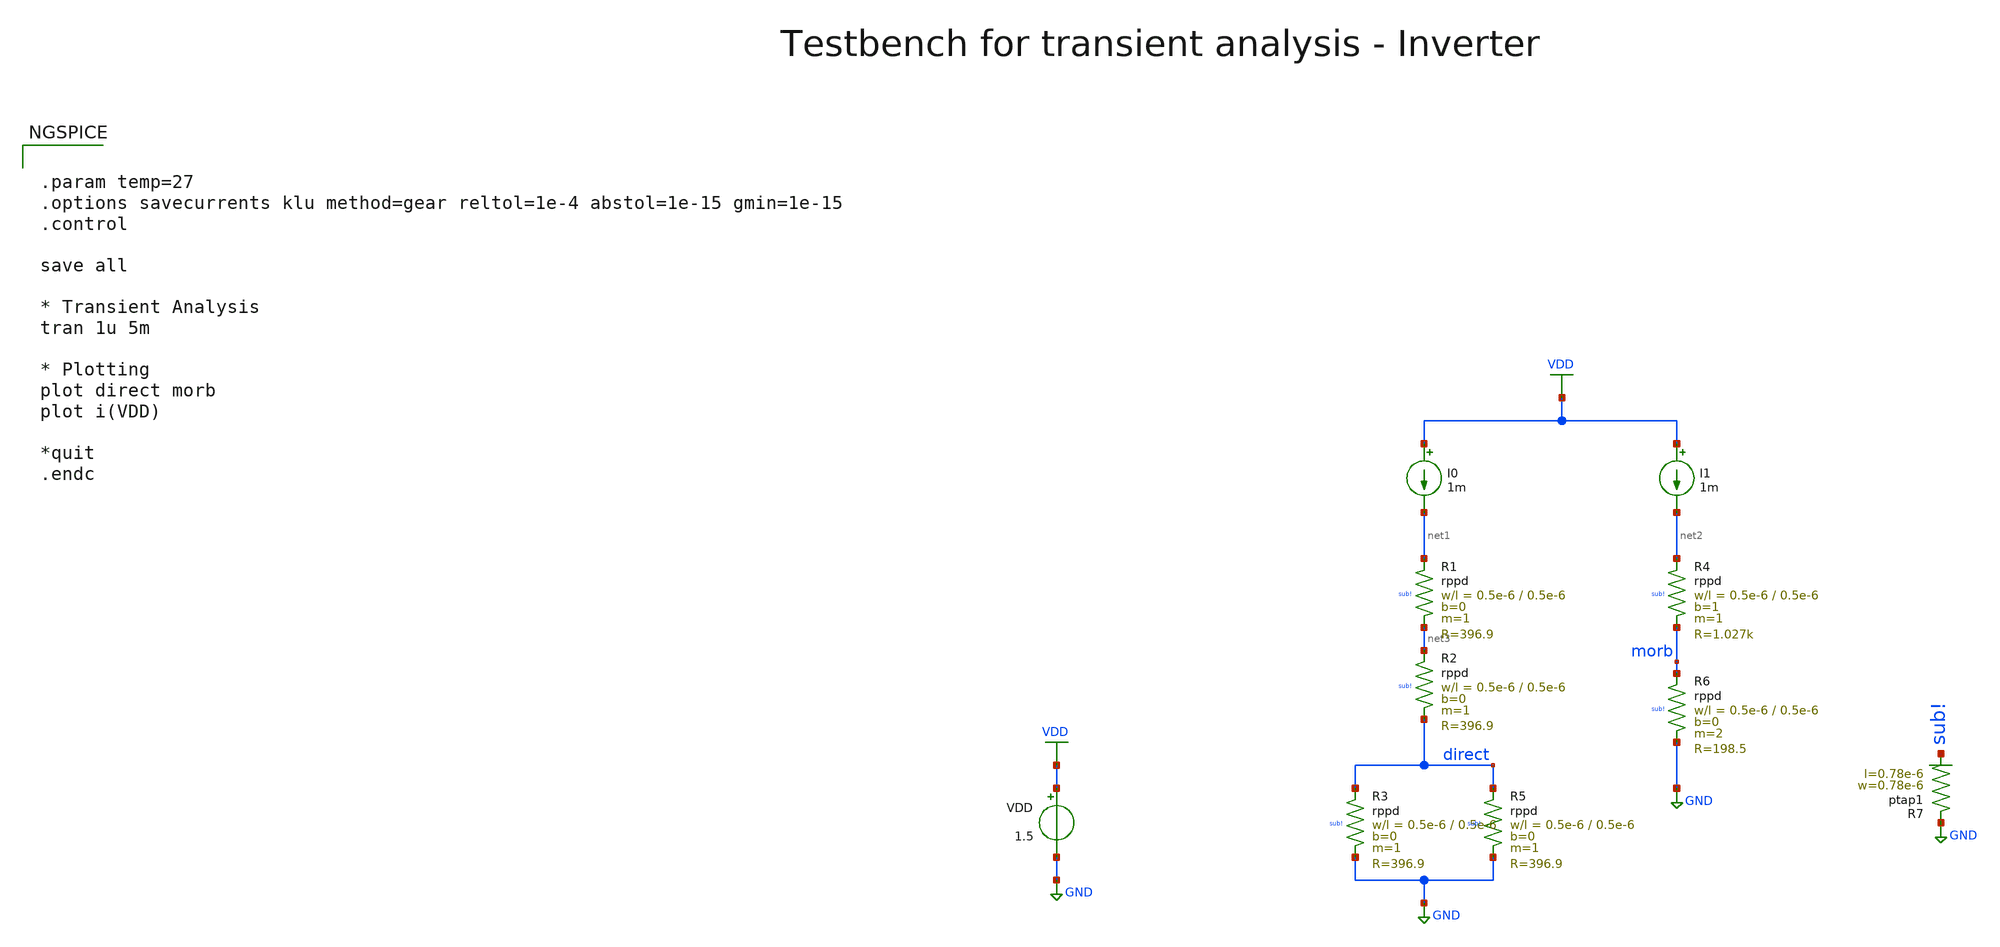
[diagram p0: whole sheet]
** sch_path: multiplier_support/testbench/rppd_tb_tran.sch
**.subckt rppd_tb_tran
VDD VDD GND 1.5
I0 VDD net1 1m
I1 VDD net2 1m
XR7 GND sub! ptap1 R=262.8 w=0.78e-6 l=0.78e-6
XR1 net1 net3 sub! rppd w=0.5e-6 l=0.5e-6 m=1 b=0 mm_ok=1
XR2 net3 direct sub! rppd w=0.5e-6 l=0.5e-6 m=1 b=0 mm_ok=1
XR3 direct GND sub! rppd w=0.5e-6 l=0.5e-6 m=1 b=0 mm_ok=1
XR5 direct GND sub! rppd w=0.5e-6 l=0.5e-6 m=1 b=0 mm_ok=1
XR4 net2 morb sub! rppd w=0.5e-6 l=0.5e-6 m=1 b=1 mm_ok=1
XR6 morb GND sub! rppd w=0.5e-6 l=0.5e-6 m=2 b=0 mm_ok=1
**** begin user architecture code


.param temp=27
.options savecurrents klu method=gear reltol=1e-4 abstol=1e-15 gmin=1e-15
.control

save all

* Transient Analysis
tran 1u 5m

* Plotting
plot direct morb
plot i(VDD)

*quit
.endc



.lib cornerMOSlv.lib mos_tt
.lib cornerMOShv.lib mos_tt
.lib cornerHBT.lib hbt_typ
.lib cornerRES.lib res_typ
.lib cornerCAP.lib cap_typ
.lib cornerDIO.lib dio_tt

**** end user architecture code
**.ends
.GLOBAL GND
.GLOBAL VDD
.end
